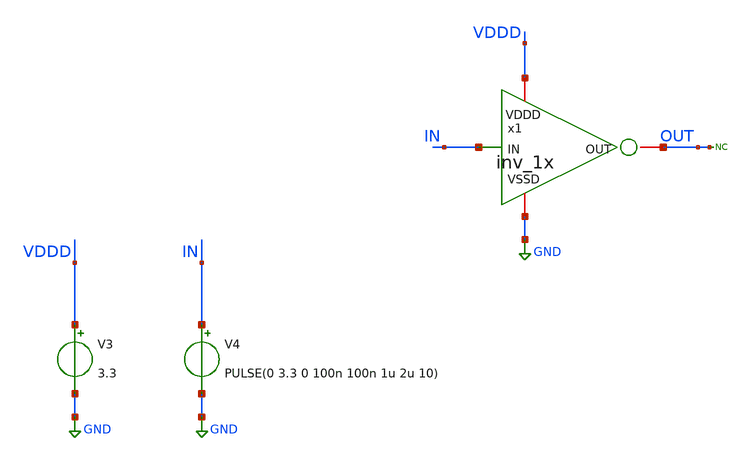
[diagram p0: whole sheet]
** sch_path: SAR_ADC/blocks/SAR_logic/inv_1x_tb.sch
**.subckt inv_1x_tb
x1 VDDD IN OUT GND inv_1x
V4 IN GND PULSE(0 3.3 0 100n 100n 1u 2u 10)
V3 VDDD GND 3.3
* noconn OUT
**** begin user architecture code



*Parameters
.options TEMPS= 27.0

*Models
.include /home/electrica/Documents/gf180_projects/pdk/gf180mcuC/libs.tech/ngspice/design.ngspice
.lib /home/electrica/Documents/gf180_projects/pdk/gf180mcuC/libs.tech/ngspice/sm141064.ngspice typical
.lib /home/electrica/Documents/gf180_projects/pdk/gf180mcuC/libs.tech/ngspice/smbb000149.ngspice typical


*Data to save
.save all

*Simulation
.control
tran 1n 10u
setplot dc1
plot V(IN)+4 V(OUT)
set filetype=ascii
write inv_1x_tb_tran.raw

reset
unset filetype
op
save all
write inv_1x_tb.raw

.endc
.end



**** end user architecture code
**.ends
.GLOBAL GND
.end
